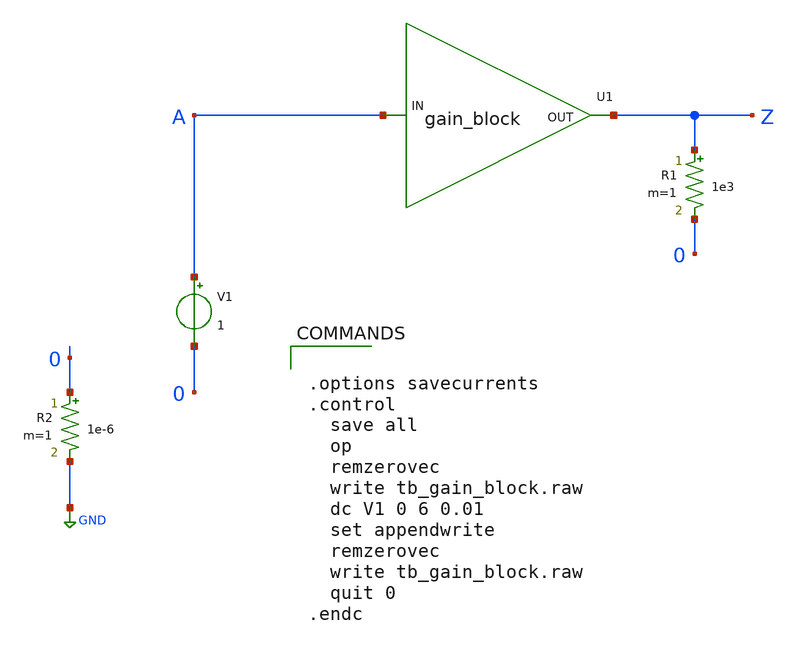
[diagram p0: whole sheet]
** sch_path: xsch/tb/tb_gain_block.sch
**.subckt tb_gain_block
V1 A 0 1
R2 0 GND 1e-6 m=1
R1 Z 0 1e3 m=1
XU1 A Z gain_block_cell
**** begin user architecture code


.options savecurrents
.control
  save all
  op
  remzerovec
  write tb_gain_block.raw
  dc V1 0 6 0.01
  set appendwrite
  remzerovec
  write tb_gain_block.raw
  quit 0
.endc


**** end user architecture code
**.ends
.GLOBAL GND
**** begin user architecture code

.subckt gain_block_cell IN OUT
N1 IN OUT gain_block_model
.ends gain_block_cell

.model gain_block_model gain_block

.control
* following line specifies the location for the .osdi file so ngspice can use it.
pre_osdi /home/vincef/projects/ttsky25b_tinychaos/xsch/veriloga/gain_block.osdi
.endc

**** end user architecture code
.end
